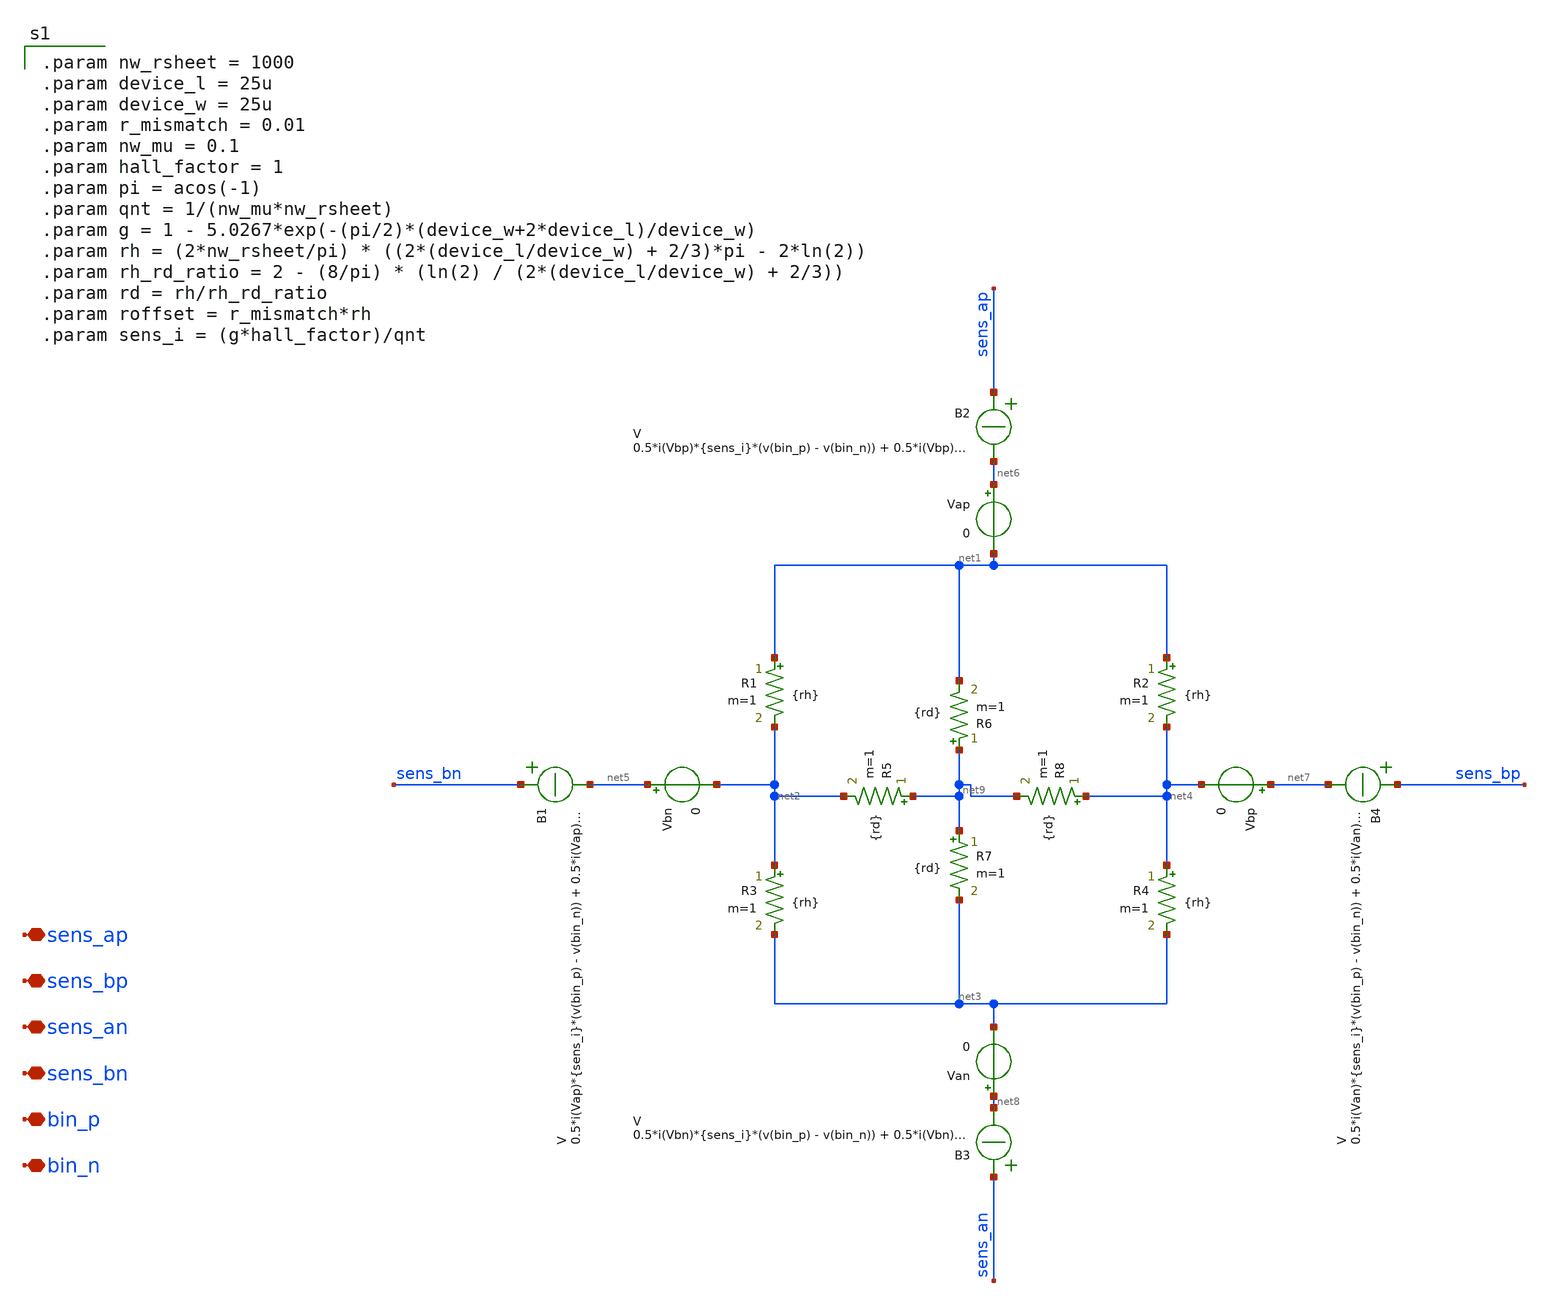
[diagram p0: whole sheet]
** sch_path: xschem/hall_plate_bhv/hall_plate_bhv.sch
**.subckt hall_plate_bhv sens_bn sens_an sens_bp sens_ap bin_p bin_n
*.iopin sens_bn
*.iopin sens_an
*.iopin sens_bp
*.iopin sens_ap
*.iopin bin_p
*.iopin bin_n
R1 net1 net2 {rh} m=1
R2 net1 net4 {rh} m=1
R3 net2 net3 {rh} m=1
R4 net4 net3 {rh} m=1
R5 net9 net2 {rd} m=1
B1 sens_bn net5 V = 0.5*i(Vap)*{sens_i}*(v(bin_p) - v(bin_n)) + 0.5*i(Vap)*{roffset}
B2 sens_ap net6 V = 0.5*i(Vbp)*{sens_i}*(v(bin_p) - v(bin_n)) + 0.5*i(Vbp)*{roffset}
B3 sens_an net8 V = 0.5*i(Vbn)*{sens_i}*(v(bin_p) - v(bin_n)) + 0.5*i(Vbn)*{roffset}
B4 sens_bp net7 V = 0.5*i(Van)*{sens_i}*(v(bin_p) - v(bin_n)) + 0.5*i(Van)*{roffset}
Vbn net5 net2 0
Vap net6 net1 0
Vbp net7 net4 0
Van net8 net3 0
R6 net9 net1 {rd} m=1
R7 net9 net3 {rd} m=1
R8 net4 net9 {rd} m=1
**** begin user architecture code

.param nw_rsheet = 1000
.param device_l = 25u
.param device_w = 25u
.param r_mismatch = 0.01
.param nw_mu = 0.1
.param hall_factor = 1
.param pi = acos(-1)
.param qnt = 1/(nw_mu*nw_rsheet)
.param g = 1 - 5.0267*exp(-(pi/2)*(device_w+2*device_l)/device_w)
.param rh = (2*nw_rsheet/pi) * ((2*(device_l/device_w) + 2/3)*pi - 2*ln(2))
.param rh_rd_ratio = 2 - (8/pi) * (ln(2) / (2*(device_l/device_w) + 2/3))
.param rd = rh/rh_rd_ratio
.param roffset = r_mismatch*rh
.param sens_i = (g*hall_factor)/qnt

**** end user architecture code
**.ends
.end
